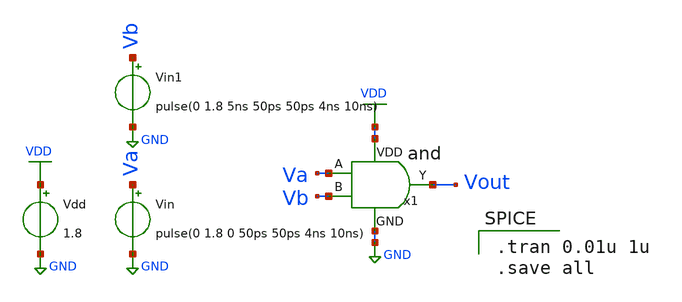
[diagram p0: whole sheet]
** sch_path: designs/inverter/xschem/untitled-1.sch
**.subckt untitled-1
Vdd VDD GND 1.8
Vin Va GND pulse(0 1.8 0 50ps 50ps 4ns 10ns)
Vin1 Vb GND pulse(0 1.8 5ns 50ps 50ps 4ns 10ns)
x1 VDD Va Vout Vb GND and
**** begin user architecture code

** opencircuidesign pdks install
.lib /home/ubvm/Desktop/chip_design/open_pdks/sky130/sky130A/libs.tech/ngspice/sky130.lib.spice tt_mm




.tran 0.01u 1u
.save all

**** end user architecture code
**.ends

* expanding   symbol:  /home/ubvm/unic-cass/and/and.sym # of pins=5
** sym_path: designs/and/xschem/and.sym
** sch_path: designs/and/xschem/and.sch
.subckt and VDD A Y B GND
input p1
output p2
inout p3
inout p4
input p5
x2 net1 net4 net3 net2 inverter
x1 net1 net5 net6 net4 net2 nand
.ends


* expanding   symbol:  inverter.sym # of pins=4
** sym_path: designs/inverter/xschem/inverter.sym
** sch_path: designs/inverter/xschem/inverter.sch
.subckt inverter VDD A Y GND
input p1
output p2
inout p3
inout p4
XM1 net1 net2 net4 net4 sky130_fd_pr__nfet_01v8 L=0.15 W=1 nf=1 ad='int((1 + 1)/2) * 1 / 1 * 0.29' as='int((1 + 2)/2) * 1 / 1 * 0.29'
+ pd='2*int((1 + 1)/2) * (1 / 1 + 0.29)' ps='2*int((1 + 2)/2) * (1 / 1 + 0.29)' nrd='0.29 / 1 ' nrs='0.29 / 1 '
+ sa=0 sb=0 sd=0 mult=1 m=1
XM2 net1 net2 net3 net3 sky130_fd_pr__pfet_01v8 L=0.15 W=1 nf=1 ad='int((1 + 1)/2) * 1 / 1 * 0.29' as='int((1 + 2)/2) * 1 / 1 * 0.29'
+ pd='2*int((1 + 1)/2) * (1 / 1 + 0.29)' ps='2*int((1 + 2)/2) * (1 / 1 + 0.29)' nrd='0.29 / 1 ' nrs='0.29 / 1 '
+ sa=0 sb=0 sd=0 mult=1 m=1
.ends


* expanding   symbol:  /home/ubvm/unic-cass/nand/nand.sym # of pins=5
** sym_path: designs/nand/xschem/nand.sym
** sch_path: designs/nand/xschem/nand.sch
.subckt nand VDD A B Y GND
input p1
input p2
output p3
inout p4
inout p5
XM1 net2 net5 net4 net4 sky130_fd_pr__nfet_01v8 L=0.15 W=1 nf=1 ad='int((1 + 1)/2) * 1 / 1 * 0.29' as='int((1 + 2)/2) * 1 / 1 * 0.29'
+ pd='2*int((1 + 1)/2) * (1 / 1 + 0.29)' ps='2*int((1 + 2)/2) * (1 / 1 + 0.29)' nrd='0.29 / 1 ' nrs='0.29 / 1 '
+ sa=0 sb=0 sd=0 mult=1 m=1
XM2 net2 net6 net1 net1 sky130_fd_pr__pfet_01v8 L=0.15 W=1 nf=1 ad='int((1 + 1)/2) * 1 / 1 * 0.29' as='int((1 + 2)/2) * 1 / 1 * 0.29'
+ pd='2*int((1 + 1)/2) * (1 / 1 + 0.29)' ps='2*int((1 + 2)/2) * (1 / 1 + 0.29)' nrd='0.29 / 1 ' nrs='0.29 / 1 '
+ sa=0 sb=0 sd=0 mult=1 m=1
XM3 net1 net5 net3 net3 sky130_fd_pr__pfet_01v8 L=0.15 W=1 nf=1 ad='int((1 + 1)/2) * 1 / 1 * 0.29' as='int((1 + 2)/2) * 1 / 1 * 0.29'
+ pd='2*int((1 + 1)/2) * (1 / 1 + 0.29)' ps='2*int((1 + 2)/2) * (1 / 1 + 0.29)' nrd='0.29 / 1 ' nrs='0.29 / 1 '
+ sa=0 sb=0 sd=0 mult=1 m=1
XM4 net2 net6 net4 net4 sky130_fd_pr__nfet_01v8 L=0.15 W=1 nf=1 ad='int((1 + 1)/2) * 1 / 1 * 0.29' as='int((1 + 2)/2) * 1 / 1 * 0.29'
+ pd='2*int((1 + 1)/2) * (1 / 1 + 0.29)' ps='2*int((1 + 2)/2) * (1 / 1 + 0.29)' nrd='0.29 / 1 ' nrs='0.29 / 1 '
+ sa=0 sb=0 sd=0 mult=1 m=1
.ends

.GLOBAL VDD
.GLOBAL GND
.end
